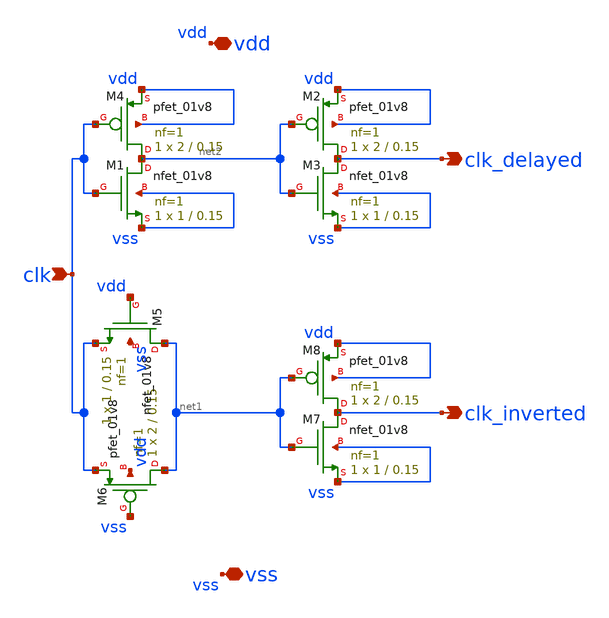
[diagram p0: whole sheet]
** sch_path: xschem/clock_phases.sch
**.subckt clock_phases clk vdd clk_delayed clk_inverted vss
*.ipin clk
*.iopin vdd
*.opin clk_delayed
*.opin clk_inverted
*.iopin vss
XM1 net2 clk vss vss sky130_fd_pr__nfet_01v8 L=0.15 W=1 nf=1 ad='int((nf+1)/2) * W/nf * 0.29' as='int((nf+2)/2) * W/nf * 0.29'
+ pd='2*int((nf+1)/2) * (W/nf + 0.29)' ps='2*int((nf+2)/2) * (W/nf + 0.29)' nrd='0.29 / W' nrs='0.29 / W'
+ sa=0 sb=0 sd=0 mult=1 m=1
XM2 clk_delayed net2 vdd vdd sky130_fd_pr__pfet_01v8 L=0.15 W=2 nf=1 ad='int((nf+1)/2) * W/nf * 0.29'
+ as='int((nf+2)/2) * W/nf * 0.29' pd='2*int((nf+1)/2) * (W/nf + 0.29)' ps='2*int((nf+2)/2) * (W/nf + 0.29)'
+ nrd='0.29 / W' nrs='0.29 / W' sa=0 sb=0 sd=0 mult=1 m=1
XM4 net2 clk vdd vdd sky130_fd_pr__pfet_01v8 L=0.15 W=2 nf=1 ad='int((nf+1)/2) * W/nf * 0.29' as='int((nf+2)/2) * W/nf * 0.29'
+ pd='2*int((nf+1)/2) * (W/nf + 0.29)' ps='2*int((nf+2)/2) * (W/nf + 0.29)' nrd='0.29 / W' nrs='0.29 / W'
+ sa=0 sb=0 sd=0 mult=1 m=1
XM8 clk_inverted net1 vdd vdd sky130_fd_pr__pfet_01v8 L=0.15 W=2 nf=1 ad='int((nf+1)/2) * W/nf * 0.29'
+ as='int((nf+2)/2) * W/nf * 0.29' pd='2*int((nf+1)/2) * (W/nf + 0.29)' ps='2*int((nf+2)/2) * (W/nf + 0.29)'
+ nrd='0.29 / W' nrs='0.29 / W' sa=0 sb=0 sd=0 mult=1 m=1
XM6 net1 vss clk vdd sky130_fd_pr__pfet_01v8 L=0.15 W=2 nf=1 ad='int((nf+1)/2) * W/nf * 0.29' as='int((nf+2)/2) * W/nf * 0.29'
+ pd='2*int((nf+1)/2) * (W/nf + 0.29)' ps='2*int((nf+2)/2) * (W/nf + 0.29)' nrd='0.29 / W' nrs='0.29 / W'
+ sa=0 sb=0 sd=0 mult=1 m=1
XM3 clk_delayed net2 vss vss sky130_fd_pr__nfet_01v8 L=0.15 W=1 nf=1 ad='int((nf+1)/2) * W/nf * 0.29'
+ as='int((nf+2)/2) * W/nf * 0.29' pd='2*int((nf+1)/2) * (W/nf + 0.29)' ps='2*int((nf+2)/2) * (W/nf + 0.29)'
+ nrd='0.29 / W' nrs='0.29 / W' sa=0 sb=0 sd=0 mult=1 m=1
XM7 clk_inverted net1 vss vss sky130_fd_pr__nfet_01v8 L=0.15 W=1 nf=1 ad='int((nf+1)/2) * W/nf * 0.29'
+ as='int((nf+2)/2) * W/nf * 0.29' pd='2*int((nf+1)/2) * (W/nf + 0.29)' ps='2*int((nf+2)/2) * (W/nf + 0.29)'
+ nrd='0.29 / W' nrs='0.29 / W' sa=0 sb=0 sd=0 mult=1 m=1
XM5 net1 vdd clk vss sky130_fd_pr__nfet_01v8 L=0.15 W=1 nf=1 ad='int((nf+1)/2) * W/nf * 0.29' as='int((nf+2)/2) * W/nf * 0.29'
+ pd='2*int((nf+1)/2) * (W/nf + 0.29)' ps='2*int((nf+2)/2) * (W/nf + 0.29)' nrd='0.29 / W' nrs='0.29 / W'
+ sa=0 sb=0 sd=0 mult=1 m=1
**.ends
.end
